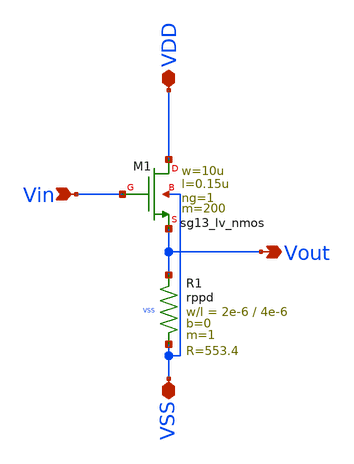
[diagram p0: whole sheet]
** sch_path: OTA_Telescopic/Schematics_and_Symbols/OTA_Output_Buffer.sch
**.subckt OTA_Output_Buffer VSS VDD Vin Vout
*.iopin VSS
*.iopin VDD
*.ipin Vin
*.opin Vout
XM1 VDD Vin Vout VSS sg13_lv_nmos w=10u l=0.15u ng=1 m=200 mm_ok=1
XR1 Vout VSS VSS rppd w=2e-6 l=4e-6 m=1 b=0 mm_ok=1
**.ends
.end
